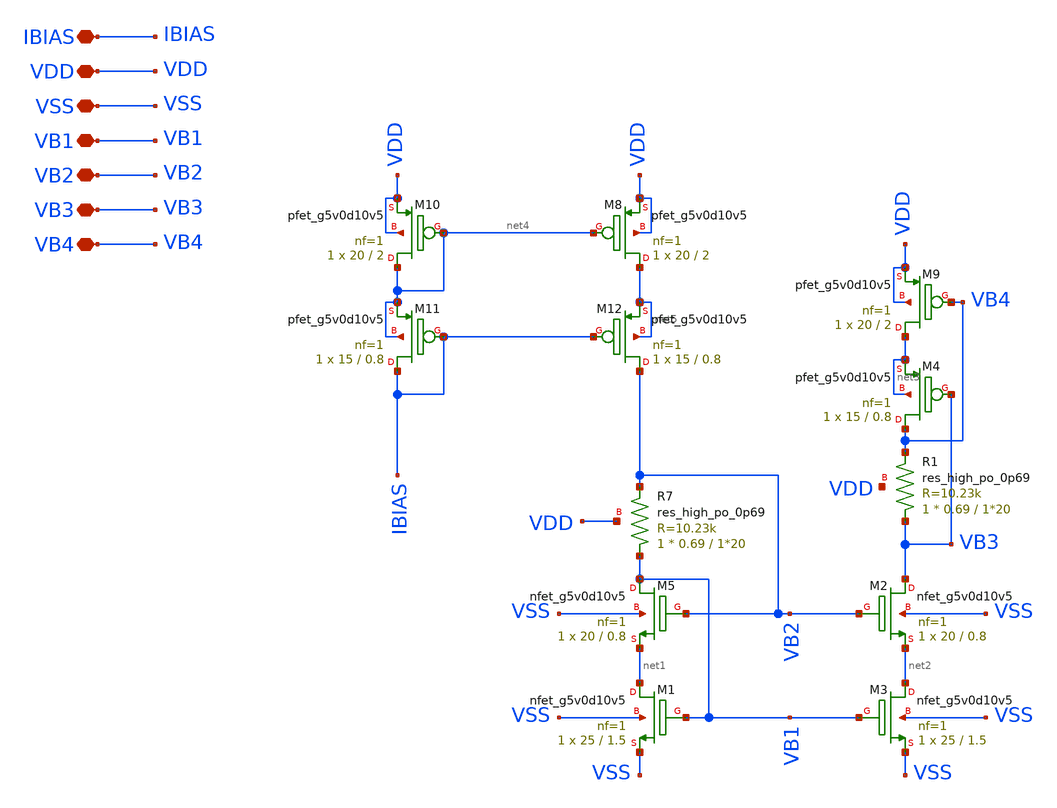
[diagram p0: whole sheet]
** sch_path: old stuff/folded_cascode_amplifier_upgraded/Low_voltage_current_mirror_NMOS/bias_generator.sch
**.subckt bias_generator IBIAS VDD VSS VB1 VB2 VB3 VB4
*.iopin IBIAS
*.iopin VDD
*.iopin VSS
*.iopin VB1
*.iopin VB2
*.iopin VB3
*.iopin VB4
XR7 VB1 VB2 VDD sky130_fd_pr__res_high_po_0p69 L=1*20 mult=1 m=1
XM5 VB1 VB2 net1 VSS sky130_fd_pr__nfet_g5v0d10v5 L=0.8 W=20 nf=1 ad='int((1 + 1)/2) * 20 / 1 * 0.29'
+ as='int((1 + 2)/2) * 20 / 1 * 0.29' pd='2*int((1 + 1)/2) * (20 / 1 + 0.29)' ps='2*int((1 + 2)/2) * (20 / 1 + 0.29)'
+ nrd='0.29 / 20 ' nrs='0.29 / 20 ' sa=0 sb=0 sd=0 mult=1 m=1
XM1 net1 VB1 VSS VSS sky130_fd_pr__nfet_g5v0d10v5 L=1.5 W=25 nf=1 ad='int((1 + 1)/2) * 25 / 1 * 0.29'
+ as='int((1 + 2)/2) * 25 / 1 * 0.29' pd='2*int((1 + 1)/2) * (25 / 1 + 0.29)' ps='2*int((1 + 2)/2) * (25 / 1 + 0.29)'
+ nrd='0.29 / 25 ' nrs='0.29 / 25 ' sa=0 sb=0 sd=0 mult=1 m=1
XM3 net2 VB1 VSS VSS sky130_fd_pr__nfet_g5v0d10v5 L=1.5 W=25 nf=1 ad='int((1 + 1)/2) * 25 / 1 * 0.29'
+ as='int((1 + 2)/2) * 25 / 1 * 0.29' pd='2*int((1 + 1)/2) * (25 / 1 + 0.29)' ps='2*int((1 + 2)/2) * (25 / 1 + 0.29)'
+ nrd='0.29 / 25 ' nrs='0.29 / 25 ' sa=0 sb=0 sd=0 mult=1 m=1
XM2 VB3 VB2 net2 VSS sky130_fd_pr__nfet_g5v0d10v5 L=0.8 W=20 nf=1 ad='int((1 + 1)/2) * 20 / 1 * 0.29'
+ as='int((1 + 2)/2) * 20 / 1 * 0.29' pd='2*int((1 + 1)/2) * (20 / 1 + 0.29)' ps='2*int((1 + 2)/2) * (20 / 1 + 0.29)'
+ nrd='0.29 / 20 ' nrs='0.29 / 20 ' sa=0 sb=0 sd=0 mult=1 m=1
XM9 net3 VB4 VDD VDD sky130_fd_pr__pfet_g5v0d10v5 L=2 W=20 nf=1 ad='int((1 + 1)/2) * 20 / 1 * 0.29' as='int((1 + 2)/2) * 20 / 1 * 0.29'
+ pd='2*int((1 + 1)/2) * (20 / 1 + 0.29)' ps='2*int((1 + 2)/2) * (20 / 1 + 0.29)' nrd='0.29 / 20 ' nrs='0.29 / 20 '
+ sa=0 sb=0 sd=0 mult=1 m=1
XM4 VB4 VB3 net3 net3 sky130_fd_pr__pfet_g5v0d10v5 L=0.8 W=15 nf=1 ad='int((1 + 1)/2) * 15 / 1 * 0.29'
+ as='int((1 + 2)/2) * 15 / 1 * 0.29' pd='2*int((1 + 1)/2) * (15 / 1 + 0.29)' ps='2*int((1 + 2)/2) * (15 / 1 + 0.29)'
+ nrd='0.29 / 15 ' nrs='0.29 / 15 ' sa=0 sb=0 sd=0 mult=1 m=1
XR1 VB3 VB4 VDD sky130_fd_pr__res_high_po_0p69 L=1*20 mult=1 m=1
XM8 net5 net4 VDD VDD sky130_fd_pr__pfet_g5v0d10v5 L=2 W=20 nf=1 ad='int((1 + 1)/2) * 20 / 1 * 0.29'
+ as='int((1 + 2)/2) * 20 / 1 * 0.29' pd='2*int((1 + 1)/2) * (20 / 1 + 0.29)' ps='2*int((1 + 2)/2) * (20 / 1 + 0.29)'
+ nrd='0.29 / 20 ' nrs='0.29 / 20 ' sa=0 sb=0 sd=0 mult=1 m=1
XM10 net4 net4 VDD VDD sky130_fd_pr__pfet_g5v0d10v5 L=2 W=20 nf=1 ad='int((1 + 1)/2) * 20 / 1 * 0.29'
+ as='int((1 + 2)/2) * 20 / 1 * 0.29' pd='2*int((1 + 1)/2) * (20 / 1 + 0.29)' ps='2*int((1 + 2)/2) * (20 / 1 + 0.29)'
+ nrd='0.29 / 20 ' nrs='0.29 / 20 ' sa=0 sb=0 sd=0 mult=1 m=1
XM11 IBIAS IBIAS net4 net4 sky130_fd_pr__pfet_g5v0d10v5 L=0.8 W=15 nf=1 ad='int((1 + 1)/2) * 15 / 1 * 0.29'
+ as='int((1 + 2)/2) * 15 / 1 * 0.29' pd='2*int((1 + 1)/2) * (15 / 1 + 0.29)' ps='2*int((1 + 2)/2) * (15 / 1 + 0.29)'
+ nrd='0.29 / 15 ' nrs='0.29 / 15 ' sa=0 sb=0 sd=0 mult=1 m=1
XM12 VB2 IBIAS net5 net5 sky130_fd_pr__pfet_g5v0d10v5 L=0.8 W=15 nf=1 ad='int((1 + 1)/2) * 15 / 1 * 0.29'
+ as='int((1 + 2)/2) * 15 / 1 * 0.29' pd='2*int((1 + 1)/2) * (15 / 1 + 0.29)' ps='2*int((1 + 2)/2) * (15 / 1 + 0.29)'
+ nrd='0.29 / 15 ' nrs='0.29 / 15 ' sa=0 sb=0 sd=0 mult=1 m=1
**.ends
.end
